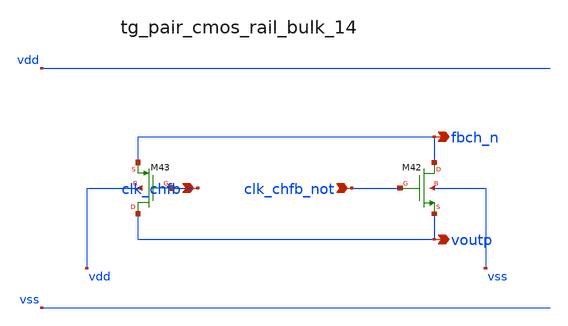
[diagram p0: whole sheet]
** sch_path: analog-db/raw/ia_003_fan_chopper_pf/hier/blocks/tg_pair_cmos_rail_bulk_14.sch
**.subckt tg_pair_cmos_rail_bulk_14 clk_chfb clk_chfb_not fbch_n voutp
*.ipin clk_chfb
*.ipin clk_chfb_not
*.opin fbch_n
*.opin voutp
XM42 fbch_n clk_chfb_not voutp vss sg13_lv_nmos w=x_dut_xm42_w l=x_dut_xm42_l ng=1 m=x_dut_xm42_m
XM43 voutp clk_chfb fbch_n vdd sg13_lv_pmos w=x_dut_xm43_w l=x_dut_xm43_l ng=1 m=x_dut_xm43_m
**.ends
.end
